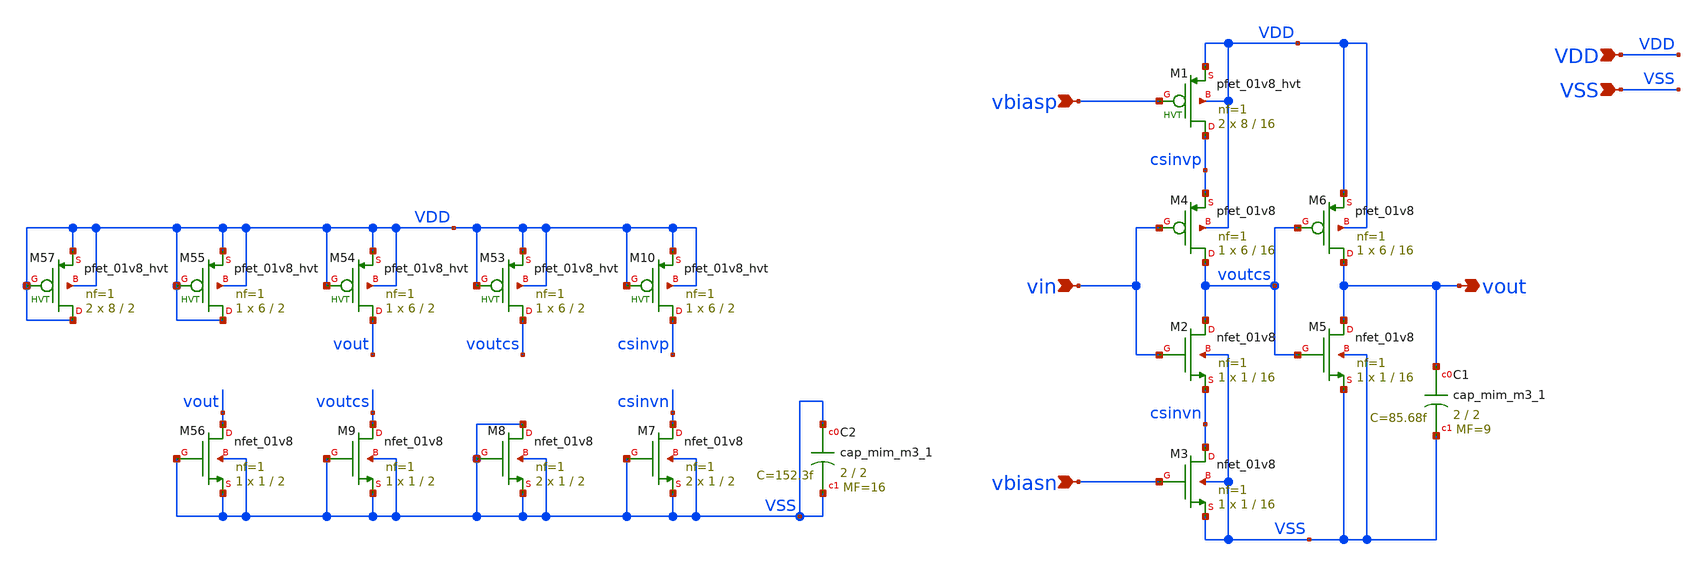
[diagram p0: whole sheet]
** sch_path: designs/cs_ring_osc_stage_lvs.sch
* Copyright 2020 Stefan Frederik Schippers
* Licensed under the Apache License, Version 2.0 (the "License");
* you may not use this file except in compliance with the License.
* You may obtain a copy of the License at
* https://www.apache.org/licenses/LICENSE-2.0
* Unless required by applicable law or agreed to in writing, software
* distributed under the License is distributed on an "AS IS" BASIS,
* WITHOUT WARRANTIES OR CONDITIONS OF ANY KIND, either express or implied.
* See the License for the specific language governing permissions and
* limitations under the License.
**.subckt cs_ring_osc_stage_lvs vout vin vbiasn vbiasp VDD VSS
*.opin vout
*.ipin vin
*.ipin vbiasn
*.ipin vbiasp
*.ipin VDD
*.ipin VSS
XM2 voutcs vin csinvn VSS sky130_fd_pr__nfet_01v8 L=16 W=1 nf=1 ad='int((nf+1)/2) * W/nf * 0.29' as='int((nf+2)/2) * W/nf * 0.29'
+ pd='2*int((nf+1)/2) * (W/nf + 0.29)' ps='2*int((nf+2)/2) * (W/nf + 0.29)' nrd='0.29 / W' nrs='0.29 / W'
+ sa=0 sb=0 sd=0 mult=1 m=1
XM4 voutcs vin csinvp VDD sky130_fd_pr__pfet_01v8 L=16 W=6 nf=1 ad='int((nf+1)/2) * W/nf * 0.29' as='int((nf+2)/2) * W/nf * 0.29'
+ pd='2*int((nf+1)/2) * (W/nf + 0.29)' ps='2*int((nf+2)/2) * (W/nf + 0.29)' nrd='0.29 / W' nrs='0.29 / W'
+ sa=0 sb=0 sd=0 mult=1 m=1
XM1 csinvp vbiasp VDD VDD sky130_fd_pr__pfet_01v8_hvt L=16 W=8 nf=1 ad='int((nf+1)/2) * W/nf * 0.29'
+ as='int((nf+2)/2) * W/nf * 0.29' pd='2*int((nf+1)/2) * (W/nf + 0.29)' ps='2*int((nf+2)/2) * (W/nf + 0.29)'
+ nrd='0.29 / W' nrs='0.29 / W' sa=0 sb=0 sd=0 mult=2 m=2
XC1 vout VSS sky130_fd_pr__cap_mim_m3_1 W=2 L=2 MF=9 m=9
XM3 csinvn vbiasn VSS VSS sky130_fd_pr__nfet_01v8 L=16 W=1 nf=1 ad='int((nf+1)/2) * W/nf * 0.29' as='int((nf+2)/2) * W/nf * 0.29'
+ pd='2*int((nf+1)/2) * (W/nf + 0.29)' ps='2*int((nf+2)/2) * (W/nf + 0.29)' nrd='0.29 / W' nrs='0.29 / W'
+ sa=0 sb=0 sd=0 mult=1 m=1
XM5 vout voutcs VSS VSS sky130_fd_pr__nfet_01v8 L=16 W=1 nf=1 ad='int((nf+1)/2) * W/nf * 0.29' as='int((nf+2)/2) * W/nf * 0.29'
+ pd='2*int((nf+1)/2) * (W/nf + 0.29)' ps='2*int((nf+2)/2) * (W/nf + 0.29)' nrd='0.29 / W' nrs='0.29 / W'
+ sa=0 sb=0 sd=0 mult=1 m=1
XM6 vout voutcs VDD VDD sky130_fd_pr__pfet_01v8 L=16 W=6 nf=1 ad='int((nf+1)/2) * W/nf * 0.29' as='int((nf+2)/2) * W/nf * 0.29'
+ pd='2*int((nf+1)/2) * (W/nf + 0.29)' ps='2*int((nf+2)/2) * (W/nf + 0.29)' nrd='0.29 / W' nrs='0.29 / W'
+ sa=0 sb=0 sd=0 mult=1 m=1
XC2 VSS VSS sky130_fd_pr__cap_mim_m3_1 W=2 L=2 MF=16 m=16
XM7 csinvn VSS VSS VSS sky130_fd_pr__nfet_01v8 L=2 W=1 nf=1 ad='int((nf+1)/2) * W/nf * 0.29' as='int((nf+2)/2) * W/nf * 0.29'
+ pd='2*int((nf+1)/2) * (W/nf + 0.29)' ps='2*int((nf+2)/2) * (W/nf + 0.29)' nrd='0.29 / W' nrs='0.29 / W'
+ sa=0 sb=0 sd=0 mult=2 m=2
XM8 VSS VSS VSS VSS sky130_fd_pr__nfet_01v8 L=2 W=1 nf=1 ad='int((nf+1)/2) * W/nf * 0.29' as='int((nf+2)/2) * W/nf * 0.29'
+ pd='2*int((nf+1)/2) * (W/nf + 0.29)' ps='2*int((nf+2)/2) * (W/nf + 0.29)' nrd='0.29 / W' nrs='0.29 / W'
+ sa=0 sb=0 sd=0 mult=2 m=2
XM9 voutcs VSS VSS VSS sky130_fd_pr__nfet_01v8 L=2 W=1 nf=1 ad='int((nf+1)/2) * W/nf * 0.29' as='int((nf+2)/2) * W/nf * 0.29'
+ pd='2*int((nf+1)/2) * (W/nf + 0.29)' ps='2*int((nf+2)/2) * (W/nf + 0.29)' nrd='0.29 / W' nrs='0.29 / W'
+ sa=0 sb=0 sd=0 mult=1 m=1
XM56 vout VSS VSS VSS sky130_fd_pr__nfet_01v8 L=2 W=1 nf=1 ad='int((nf+1)/2) * W/nf * 0.29' as='int((nf+2)/2) * W/nf * 0.29'
+ pd='2*int((nf+1)/2) * (W/nf + 0.29)' ps='2*int((nf+2)/2) * (W/nf + 0.29)' nrd='0.29 / W' nrs='0.29 / W'
+ sa=0 sb=0 sd=0 mult=1 m=1
XM10 csinvp VDD VDD VDD sky130_fd_pr__pfet_01v8_hvt L=2 W=6 nf=1 ad='int((nf+1)/2) * W/nf * 0.29' as='int((nf+2)/2) * W/nf * 0.29'
+ pd='2*int((nf+1)/2) * (W/nf + 0.29)' ps='2*int((nf+2)/2) * (W/nf + 0.29)' nrd='0.29 / W' nrs='0.29 / W'
+ sa=0 sb=0 sd=0 mult=1 m=1
XM53 voutcs VDD VDD VDD sky130_fd_pr__pfet_01v8_hvt L=2 W=6 nf=1 ad='int((nf+1)/2) * W/nf * 0.29' as='int((nf+2)/2) * W/nf * 0.29'
+ pd='2*int((nf+1)/2) * (W/nf + 0.29)' ps='2*int((nf+2)/2) * (W/nf + 0.29)' nrd='0.29 / W' nrs='0.29 / W'
+ sa=0 sb=0 sd=0 mult=1 m=1
XM54 vout VDD VDD VDD sky130_fd_pr__pfet_01v8_hvt L=2 W=6 nf=1 ad='int((nf+1)/2) * W/nf * 0.29' as='int((nf+2)/2) * W/nf * 0.29'
+ pd='2*int((nf+1)/2) * (W/nf + 0.29)' ps='2*int((nf+2)/2) * (W/nf + 0.29)' nrd='0.29 / W' nrs='0.29 / W'
+ sa=0 sb=0 sd=0 mult=1 m=1
XM55 VDD VDD VDD VDD sky130_fd_pr__pfet_01v8_hvt L=2 W=6 nf=1 ad='int((nf+1)/2) * W/nf * 0.29' as='int((nf+2)/2) * W/nf * 0.29'
+ pd='2*int((nf+1)/2) * (W/nf + 0.29)' ps='2*int((nf+2)/2) * (W/nf + 0.29)' nrd='0.29 / W' nrs='0.29 / W'
+ sa=0 sb=0 sd=0 mult=1 m=1
XM57 VDD VDD VDD VDD sky130_fd_pr__pfet_01v8_hvt L=2 W=8 nf=1 ad='int((nf+1)/2) * W/nf * 0.29' as='int((nf+2)/2) * W/nf * 0.29'
+ pd='2*int((nf+1)/2) * (W/nf + 0.29)' ps='2*int((nf+2)/2) * (W/nf + 0.29)' nrd='0.29 / W' nrs='0.29 / W'
+ sa=0 sb=0 sd=0 mult=2 m=2
**.ends
.end
